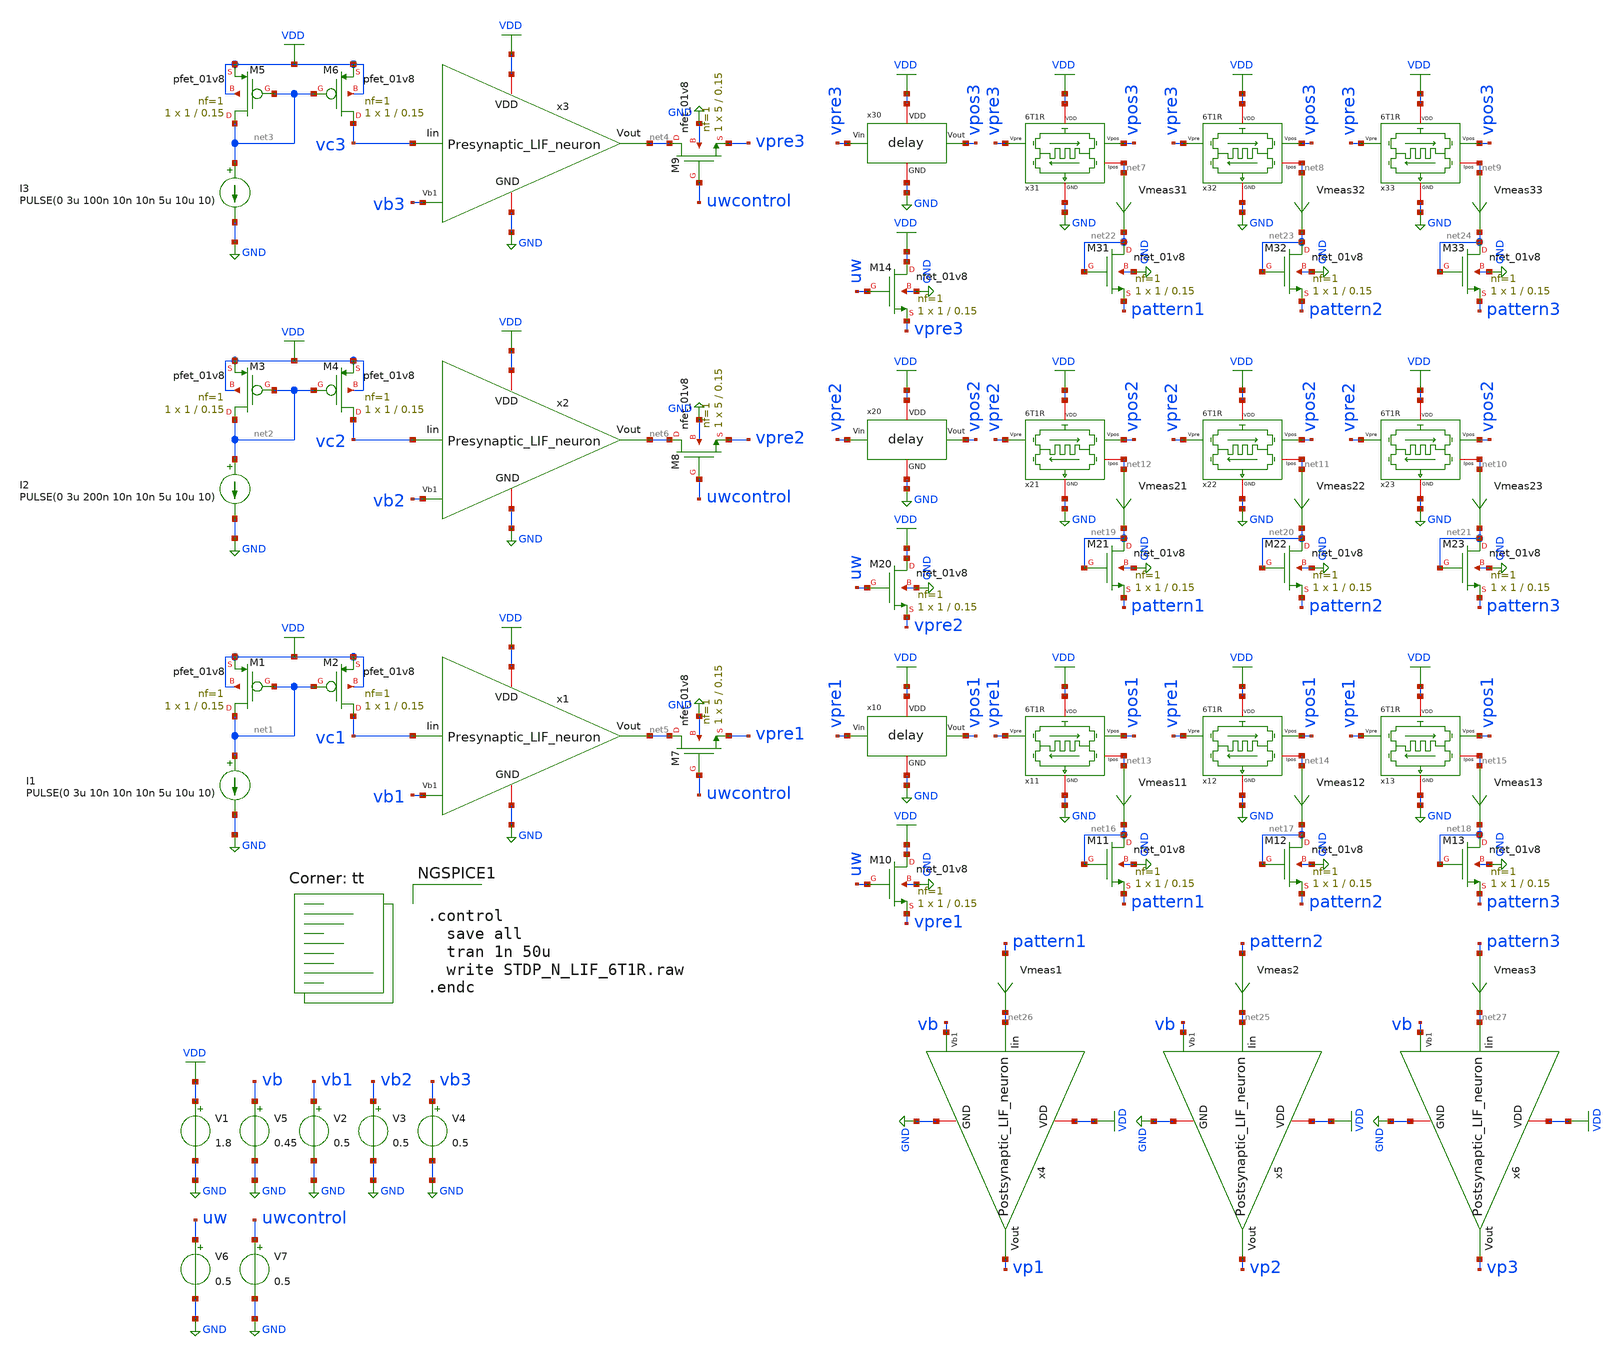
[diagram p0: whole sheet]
** sch_path: STDP/SNN_test.sch
**.subckt SNN_test
V1 VDD GND 1.8
V2 vb1 GND 0.5
I1 net1 GND PULSE(0 3u 10n 10n 10n 5u 10u 10)
XM2 vc1 net1 VDD VDD sky130_fd_pr__pfet_01v8 L=0.15 W=1 nf=1 ad='int((nf+1)/2) * W/nf * 0.29' as='int((nf+2)/2) * W/nf * 0.29'
+ pd='2*int((nf+1)/2) * (W/nf + 0.29)' ps='2*int((nf+2)/2) * (W/nf + 0.29)' nrd='0.29 / W' nrs='0.29 / W'
+ sa=0 sb=0 sd=0 mult=1 m=1
XM1 net1 net1 VDD VDD sky130_fd_pr__pfet_01v8 L=0.15 W=1 nf=1 ad='int((nf+1)/2) * W/nf * 0.29' as='int((nf+2)/2) * W/nf * 0.29'
+ pd='2*int((nf+1)/2) * (W/nf + 0.29)' ps='2*int((nf+2)/2) * (W/nf + 0.29)' nrd='0.29 / W' nrs='0.29 / W'
+ sa=0 sb=0 sd=0 mult=1 m=1
Vmeas31 net7 net22 0
.save i(vmeas31)
V3 vb2 GND 0.5
V4 vb3 GND 0.5
x1 VDD net5 vb1 GND vc1 Presynaptic_LIF_neuron
x5 net25 VDD vp2 vb GND Postsynaptic_LIF_neuron
V5 vb GND 0.45
x2 VDD net6 vb2 GND vc2 Presynaptic_LIF_neuron
I2 net2 GND PULSE(0 3u 200n 10n 10n 5u 10u 10)
XM4 vc2 net2 VDD VDD sky130_fd_pr__pfet_01v8 L=0.15 W=1 nf=1 ad='int((nf+1)/2) * W/nf * 0.29' as='int((nf+2)/2) * W/nf * 0.29'
+ pd='2*int((nf+1)/2) * (W/nf + 0.29)' ps='2*int((nf+2)/2) * (W/nf + 0.29)' nrd='0.29 / W' nrs='0.29 / W'
+ sa=0 sb=0 sd=0 mult=1 m=1
XM3 net2 net2 VDD VDD sky130_fd_pr__pfet_01v8 L=0.15 W=1 nf=1 ad='int((nf+1)/2) * W/nf * 0.29' as='int((nf+2)/2) * W/nf * 0.29'
+ pd='2*int((nf+1)/2) * (W/nf + 0.29)' ps='2*int((nf+2)/2) * (W/nf + 0.29)' nrd='0.29 / W' nrs='0.29 / W'
+ sa=0 sb=0 sd=0 mult=1 m=1
x31 VDD net7 vpre3 vpos3 GND 6T1R
x3 VDD net4 vb3 GND vc3 Presynaptic_LIF_neuron
I3 net3 GND PULSE(0 3u 100n 10n 10n 5u 10u 10)
XM6 vc3 net3 VDD VDD sky130_fd_pr__pfet_01v8 L=0.15 W=1 nf=1 ad='int((nf+1)/2) * W/nf * 0.29' as='int((nf+2)/2) * W/nf * 0.29'
+ pd='2*int((nf+1)/2) * (W/nf + 0.29)' ps='2*int((nf+2)/2) * (W/nf + 0.29)' nrd='0.29 / W' nrs='0.29 / W'
+ sa=0 sb=0 sd=0 mult=1 m=1
XM5 net3 net3 VDD VDD sky130_fd_pr__pfet_01v8 L=0.15 W=1 nf=1 ad='int((nf+1)/2) * W/nf * 0.29' as='int((nf+2)/2) * W/nf * 0.29'
+ pd='2*int((nf+1)/2) * (W/nf + 0.29)' ps='2*int((nf+2)/2) * (W/nf + 0.29)' nrd='0.29 / W' nrs='0.29 / W'
+ sa=0 sb=0 sd=0 mult=1 m=1
x30 VDD vpre3 vpos3 GND delay
XM9 net4 uwcontrol vpre3 GND sky130_fd_pr__nfet_01v8 L=0.15 W=5 nf=1 ad='int((nf+1)/2) * W/nf * 0.29'
+ as='int((nf+2)/2) * W/nf * 0.29' pd='2*int((nf+1)/2) * (W/nf + 0.29)' ps='2*int((nf+2)/2) * (W/nf + 0.29)'
+ nrd='0.29 / W' nrs='0.29 / W' sa=0 sb=0 sd=0 mult=1 m=1
XM8 net6 uwcontrol vpre2 GND sky130_fd_pr__nfet_01v8 L=0.15 W=5 nf=1 ad='int((nf+1)/2) * W/nf * 0.29'
+ as='int((nf+2)/2) * W/nf * 0.29' pd='2*int((nf+1)/2) * (W/nf + 0.29)' ps='2*int((nf+2)/2) * (W/nf + 0.29)'
+ nrd='0.29 / W' nrs='0.29 / W' sa=0 sb=0 sd=0 mult=1 m=1
XM7 net5 uwcontrol vpre1 GND sky130_fd_pr__nfet_01v8 L=0.15 W=5 nf=1 ad='int((nf+1)/2) * W/nf * 0.29'
+ as='int((nf+2)/2) * W/nf * 0.29' pd='2*int((nf+1)/2) * (W/nf + 0.29)' ps='2*int((nf+2)/2) * (W/nf + 0.29)'
+ nrd='0.29 / W' nrs='0.29 / W' sa=0 sb=0 sd=0 mult=1 m=1
x11 VDD net13 vpre1 vpos1 GND 6T1R
x10 VDD vpre1 vpos1 GND delay
x21 VDD net12 vpre2 vpos2 GND 6T1R
x20 VDD vpre2 vpos2 GND delay
x32 VDD net8 vpre3 vpos3 GND 6T1R
x12 VDD net14 vpre1 vpos1 GND 6T1R
x22 VDD net11 vpre2 vpos2 GND 6T1R
x33 VDD net9 vpre3 vpos3 GND 6T1R
x13 VDD net15 vpre1 vpos1 GND 6T1R
x23 VDD net10 vpre2 vpos2 GND 6T1R
Vmeas32 net8 net23 0
.save i(vmeas32)
Vmeas33 net9 net24 0
.save i(vmeas33)
Vmeas23 net10 net21 0
.save i(vmeas23)
Vmeas22 net11 net20 0
.save i(vmeas22)
Vmeas21 net12 net19 0
.save i(vmeas21)
Vmeas11 net13 net16 0
.save i(vmeas11)
Vmeas12 net14 net17 0
.save i(vmeas12)
Vmeas13 net15 net18 0
.save i(vmeas13)
XM11 net16 net16 pattern1 GND sky130_fd_pr__nfet_01v8 L=0.15 W=1 nf=1 ad='int((nf+1)/2) * W/nf * 0.29'
+ as='int((nf+2)/2) * W/nf * 0.29' pd='2*int((nf+1)/2) * (W/nf + 0.29)' ps='2*int((nf+2)/2) * (W/nf + 0.29)'
+ nrd='0.29 / W' nrs='0.29 / W' sa=0 sb=0 sd=0 mult=1 m=1
XM12 net17 net17 pattern2 GND sky130_fd_pr__nfet_01v8 L=0.15 W=1 nf=1 ad='int((nf+1)/2) * W/nf * 0.29'
+ as='int((nf+2)/2) * W/nf * 0.29' pd='2*int((nf+1)/2) * (W/nf + 0.29)' ps='2*int((nf+2)/2) * (W/nf + 0.29)'
+ nrd='0.29 / W' nrs='0.29 / W' sa=0 sb=0 sd=0 mult=1 m=1
XM13 net18 net18 pattern3 GND sky130_fd_pr__nfet_01v8 L=0.15 W=1 nf=1 ad='int((nf+1)/2) * W/nf * 0.29'
+ as='int((nf+2)/2) * W/nf * 0.29' pd='2*int((nf+1)/2) * (W/nf + 0.29)' ps='2*int((nf+2)/2) * (W/nf + 0.29)'
+ nrd='0.29 / W' nrs='0.29 / W' sa=0 sb=0 sd=0 mult=1 m=1
XM21 net19 net19 pattern1 GND sky130_fd_pr__nfet_01v8 L=0.15 W=1 nf=1 ad='int((nf+1)/2) * W/nf * 0.29'
+ as='int((nf+2)/2) * W/nf * 0.29' pd='2*int((nf+1)/2) * (W/nf + 0.29)' ps='2*int((nf+2)/2) * (W/nf + 0.29)'
+ nrd='0.29 / W' nrs='0.29 / W' sa=0 sb=0 sd=0 mult=1 m=1
XM22 net20 net20 pattern2 GND sky130_fd_pr__nfet_01v8 L=0.15 W=1 nf=1 ad='int((nf+1)/2) * W/nf * 0.29'
+ as='int((nf+2)/2) * W/nf * 0.29' pd='2*int((nf+1)/2) * (W/nf + 0.29)' ps='2*int((nf+2)/2) * (W/nf + 0.29)'
+ nrd='0.29 / W' nrs='0.29 / W' sa=0 sb=0 sd=0 mult=1 m=1
XM23 net21 net21 pattern3 GND sky130_fd_pr__nfet_01v8 L=0.15 W=1 nf=1 ad='int((nf+1)/2) * W/nf * 0.29'
+ as='int((nf+2)/2) * W/nf * 0.29' pd='2*int((nf+1)/2) * (W/nf + 0.29)' ps='2*int((nf+2)/2) * (W/nf + 0.29)'
+ nrd='0.29 / W' nrs='0.29 / W' sa=0 sb=0 sd=0 mult=1 m=1
XM31 net22 net22 pattern1 GND sky130_fd_pr__nfet_01v8 L=0.15 W=1 nf=1 ad='int((nf+1)/2) * W/nf * 0.29'
+ as='int((nf+2)/2) * W/nf * 0.29' pd='2*int((nf+1)/2) * (W/nf + 0.29)' ps='2*int((nf+2)/2) * (W/nf + 0.29)'
+ nrd='0.29 / W' nrs='0.29 / W' sa=0 sb=0 sd=0 mult=1 m=1
XM32 net23 net23 pattern2 GND sky130_fd_pr__nfet_01v8 L=0.15 W=1 nf=1 ad='int((nf+1)/2) * W/nf * 0.29'
+ as='int((nf+2)/2) * W/nf * 0.29' pd='2*int((nf+1)/2) * (W/nf + 0.29)' ps='2*int((nf+2)/2) * (W/nf + 0.29)'
+ nrd='0.29 / W' nrs='0.29 / W' sa=0 sb=0 sd=0 mult=1 m=1
XM33 net24 net24 pattern3 GND sky130_fd_pr__nfet_01v8 L=0.15 W=1 nf=1 ad='int((nf+1)/2) * W/nf * 0.29'
+ as='int((nf+2)/2) * W/nf * 0.29' pd='2*int((nf+1)/2) * (W/nf + 0.29)' ps='2*int((nf+2)/2) * (W/nf + 0.29)'
+ nrd='0.29 / W' nrs='0.29 / W' sa=0 sb=0 sd=0 mult=1 m=1
XM10 VDD uw vpre1 GND sky130_fd_pr__nfet_01v8 L=0.15 W=1 nf=1 ad='int((nf+1)/2) * W/nf * 0.29' as='int((nf+2)/2) * W/nf * 0.29'
+ pd='2*int((nf+1)/2) * (W/nf + 0.29)' ps='2*int((nf+2)/2) * (W/nf + 0.29)' nrd='0.29 / W' nrs='0.29 / W'
+ sa=0 sb=0 sd=0 mult=1 m=1
XM20 VDD uw vpre2 GND sky130_fd_pr__nfet_01v8 L=0.15 W=1 nf=1 ad='int((nf+1)/2) * W/nf * 0.29' as='int((nf+2)/2) * W/nf * 0.29'
+ pd='2*int((nf+1)/2) * (W/nf + 0.29)' ps='2*int((nf+2)/2) * (W/nf + 0.29)' nrd='0.29 / W' nrs='0.29 / W'
+ sa=0 sb=0 sd=0 mult=1 m=1
XM14 VDD uw vpre3 GND sky130_fd_pr__nfet_01v8 L=0.15 W=1 nf=1 ad='int((nf+1)/2) * W/nf * 0.29' as='int((nf+2)/2) * W/nf * 0.29'
+ pd='2*int((nf+1)/2) * (W/nf + 0.29)' ps='2*int((nf+2)/2) * (W/nf + 0.29)' nrd='0.29 / W' nrs='0.29 / W'
+ sa=0 sb=0 sd=0 mult=1 m=1
Vmeas2 pattern2 net25 0
.save i(vmeas2)
x4 net26 VDD vp1 vb GND Postsynaptic_LIF_neuron
Vmeas1 pattern1 net26 0
.save i(vmeas1)
x6 net27 VDD vp3 vb GND Postsynaptic_LIF_neuron
Vmeas3 pattern3 net27 0
.save i(vmeas3)
V6 uw GND 0.5
V7 uwcontrol GND 0.5
**** begin user architecture code
.lib $::SKYWATER_MODELS/sky130.lib.spice tt

** opencircuitdesign pdks install
.inc $::SKYWATER_MODELS/rram_v0.spice



.control
  save all
  tran 1n 50u
  write STDP_N_LIF_6T1R.raw
.endc


**** end user architecture code
**.ends

* expanding   symbol:
*+  /home/ricardo/RATT_repos/Proyectos_xschem/LIF_neuron/Presynaptic_LIF_neuron.sym # of pins=5
** sym_path: LIF_neuron/Presynaptic_LIF_neuron.sym
** sch_path: LIF_neuron/Presynaptic_LIF_neuron.sch
.subckt Presynaptic_LIF_neuron VDD Vout Vb1 GND Iin
*.iopin GND
*.ipin Vb1
*.iopin VDD
*.opin Vout
*.ipin Iin
XM13 net2 Vb1 GND GND sky130_fd_pr__nfet_01v8 L=0.5 W=5 nf=1 ad='int((nf+1)/2) * W/nf * 0.29' as='int((nf+2)/2) * W/nf * 0.29'
+ pd='2*int((nf+1)/2) * (W/nf + 0.29)' ps='2*int((nf+2)/2) * (W/nf + 0.29)' nrd='0.29 / W' nrs='0.29 / W'
+ sa=0 sb=0 sd=0 mult=1 m=1
XM12 Crefr net1 net2 GND sky130_fd_pr__nfet_01v8 L=1 W=1 nf=1 ad='int((nf+1)/2) * W/nf * 0.29' as='int((nf+2)/2) * W/nf * 0.29'
+ pd='2*int((nf+1)/2) * (W/nf + 0.29)' ps='2*int((nf+2)/2) * (W/nf + 0.29)' nrd='0.29 / W' nrs='0.29 / W'
+ sa=0 sb=0 sd=0 mult=1 m=1
XM11 Crefr net1 VDD VDD sky130_fd_pr__pfet_01v8 L=1 W=1 nf=1 ad='int((nf+1)/2) * W/nf * 0.29' as='int((nf+2)/2) * W/nf * 0.29'
+ pd='2*int((nf+1)/2) * (W/nf + 0.29)' ps='2*int((nf+2)/2) * (W/nf + 0.29)' nrd='0.29 / W' nrs='0.29 / W'
+ sa=0 sb=0 sd=0 mult=1 m=1
XCrefr Crefr GND sky130_fd_pr__cap_mim_m3_1 W=10 L=1 MF=1 m=1
XM14 Iin Crefr GND GND sky130_fd_pr__nfet_01v8 L=7 W=0.45 nf=1 ad='int((nf+1)/2) * W/nf * 0.29' as='int((nf+2)/2) * W/nf * 0.29'
+ pd='2*int((nf+1)/2) * (W/nf + 0.29)' ps='2*int((nf+2)/2) * (W/nf + 0.29)' nrd='0.29 / W' nrs='0.29 / W'
+ sa=0 sb=0 sd=0 mult=1 m=1
XCm Iin GND sky130_fd_pr__cap_mim_m3_1 W=10 L=1 MF=10 m=10
XM6 net3 Vout GND GND sky130_fd_pr__nfet_01v8 L=0.5 W=1 nf=1 ad='int((nf+1)/2) * W/nf * 0.29' as='int((nf+2)/2) * W/nf * 0.29'
+ pd='2*int((nf+1)/2) * (W/nf + 0.29)' ps='2*int((nf+2)/2) * (W/nf + 0.29)' nrd='0.29 / W' nrs='0.29 / W'
+ sa=0 sb=0 sd=0 mult=1 m=1
XM7 net1 Iin net3 GND sky130_fd_pr__nfet_01v8 L=1 W=1 nf=1 ad='int((nf+1)/2) * W/nf * 0.29' as='int((nf+2)/2) * W/nf * 0.29'
+ pd='2*int((nf+1)/2) * (W/nf + 0.29)' ps='2*int((nf+2)/2) * (W/nf + 0.29)' nrd='0.29 / W' nrs='0.29 / W'
+ sa=0 sb=0 sd=0 mult=1 m=1
XM8 net1 Iin VDD VDD sky130_fd_pr__pfet_01v8 L=1 W=1 nf=1 ad='int((nf+1)/2) * W/nf * 0.29' as='int((nf+2)/2) * W/nf * 0.29'
+ pd='2*int((nf+1)/2) * (W/nf + 0.29)' ps='2*int((nf+2)/2) * (W/nf + 0.29)' nrd='0.29 / W' nrs='0.29 / W'
+ sa=0 sb=0 sd=0 mult=1 m=1
XM9 Vout net1 net3 GND sky130_fd_pr__nfet_01v8 L=1 W=1 nf=1 ad='int((nf+1)/2) * W/nf * 0.29' as='int((nf+2)/2) * W/nf * 0.29'
+ pd='2*int((nf+1)/2) * (W/nf + 0.29)' ps='2*int((nf+2)/2) * (W/nf + 0.29)' nrd='0.29 / W' nrs='0.29 / W'
+ sa=0 sb=0 sd=0 mult=1 m=1
XM10 Vout net1 VDD VDD sky130_fd_pr__pfet_01v8 L=1 W=5 nf=1 ad='int((nf+1)/2) * W/nf * 0.29' as='int((nf+2)/2) * W/nf * 0.29'
+ pd='2*int((nf+1)/2) * (W/nf + 0.29)' ps='2*int((nf+2)/2) * (W/nf + 0.29)' nrd='0.29 / W' nrs='0.29 / W'
+ sa=0 sb=0 sd=0 mult=1 m=1
.ends


* expanding   symbol:
*+  /home/ricardo/RATT_repos/Proyectos_xschem/LIF_neuron/Postsynaptic_LIF_neuron.sym # of pins=5
** sym_path: LIF_neuron/Postsynaptic_LIF_neuron.sym
** sch_path: LIF_neuron/Postsynaptic_LIF_neuron.sch
.subckt Postsynaptic_LIF_neuron Iin VDD Vout Vb1 GND
*.iopin GND
*.ipin Vb1
*.iopin VDD
*.opin Vout
*.ipin Iin
XM13 net2 Vb1 GND GND sky130_fd_pr__nfet_01v8 L=0.5 W=5 nf=1 ad='int((nf+1)/2) * W/nf * 0.29' as='int((nf+2)/2) * W/nf * 0.29'
+ pd='2*int((nf+1)/2) * (W/nf + 0.29)' ps='2*int((nf+2)/2) * (W/nf + 0.29)' nrd='0.29 / W' nrs='0.29 / W'
+ sa=0 sb=0 sd=0 mult=1 m=1
XM12 Crefr net1 net2 GND sky130_fd_pr__nfet_01v8 L=1 W=1 nf=1 ad='int((nf+1)/2) * W/nf * 0.29' as='int((nf+2)/2) * W/nf * 0.29'
+ pd='2*int((nf+1)/2) * (W/nf + 0.29)' ps='2*int((nf+2)/2) * (W/nf + 0.29)' nrd='0.29 / W' nrs='0.29 / W'
+ sa=0 sb=0 sd=0 mult=1 m=1
XM11 Crefr net1 VDD VDD sky130_fd_pr__pfet_01v8 L=1 W=1 nf=1 ad='int((nf+1)/2) * W/nf * 0.29' as='int((nf+2)/2) * W/nf * 0.29'
+ pd='2*int((nf+1)/2) * (W/nf + 0.29)' ps='2*int((nf+2)/2) * (W/nf + 0.29)' nrd='0.29 / W' nrs='0.29 / W'
+ sa=0 sb=0 sd=0 mult=1 m=1
XC1 Crefr GND sky130_fd_pr__cap_mim_m3_1 W=21 L=1 MF=1 m=1
XM14 Iin Crefr GND GND sky130_fd_pr__nfet_01v8 L=40 W=1 nf=1 ad='int((nf+1)/2) * W/nf * 0.29' as='int((nf+2)/2) * W/nf * 0.29'
+ pd='2*int((nf+1)/2) * (W/nf + 0.29)' ps='2*int((nf+2)/2) * (W/nf + 0.29)' nrd='0.29 / W' nrs='0.29 / W'
+ sa=0 sb=0 sd=0 mult=1 m=1
XC2 Iin GND sky130_fd_pr__cap_mim_m3_1 W=20 L=1 MF=50 m=50
XM6 net3 Vout GND GND sky130_fd_pr__nfet_01v8 L=0.5 W=1 nf=1 ad='int((nf+1)/2) * W/nf * 0.29' as='int((nf+2)/2) * W/nf * 0.29'
+ pd='2*int((nf+1)/2) * (W/nf + 0.29)' ps='2*int((nf+2)/2) * (W/nf + 0.29)' nrd='0.29 / W' nrs='0.29 / W'
+ sa=0 sb=0 sd=0 mult=1 m=1
XM7 net1 Iin net3 GND sky130_fd_pr__nfet_01v8 L=1 W=1 nf=1 ad='int((nf+1)/2) * W/nf * 0.29' as='int((nf+2)/2) * W/nf * 0.29'
+ pd='2*int((nf+1)/2) * (W/nf + 0.29)' ps='2*int((nf+2)/2) * (W/nf + 0.29)' nrd='0.29 / W' nrs='0.29 / W'
+ sa=0 sb=0 sd=0 mult=1 m=1
XM8 net1 Iin VDD VDD sky130_fd_pr__pfet_01v8 L=1 W=1 nf=1 ad='int((nf+1)/2) * W/nf * 0.29' as='int((nf+2)/2) * W/nf * 0.29'
+ pd='2*int((nf+1)/2) * (W/nf + 0.29)' ps='2*int((nf+2)/2) * (W/nf + 0.29)' nrd='0.29 / W' nrs='0.29 / W'
+ sa=0 sb=0 sd=0 mult=1 m=1
XM9 Vout net1 net3 GND sky130_fd_pr__nfet_01v8 L=1 W=1 nf=1 ad='int((nf+1)/2) * W/nf * 0.29' as='int((nf+2)/2) * W/nf * 0.29'
+ pd='2*int((nf+1)/2) * (W/nf + 0.29)' ps='2*int((nf+2)/2) * (W/nf + 0.29)' nrd='0.29 / W' nrs='0.29 / W'
+ sa=0 sb=0 sd=0 mult=1 m=1
XM10 Vout net1 VDD VDD sky130_fd_pr__pfet_01v8 L=1 W=5 nf=1 ad='int((nf+1)/2) * W/nf * 0.29' as='int((nf+2)/2) * W/nf * 0.29'
+ pd='2*int((nf+1)/2) * (W/nf + 0.29)' ps='2*int((nf+2)/2) * (W/nf + 0.29)' nrd='0.29 / W' nrs='0.29 / W'
+ sa=0 sb=0 sd=0 mult=1 m=1
.ends


* expanding   symbol:  /home/ricardo/RATT_repos/Proyectos_xschem/synapse/6T1R.sym # of pins=5
** sym_path: synapse/6T1R.sym
** sch_path: synapse/6T1R.sch
.subckt 6T1R VDD Ipos Vpre Vpos GND
*.ipin Vpre
*.ipin Vpos
*.iopin GND
*.iopin Ipos
*.iopin VDD
XM1 BE Vpre vipre GND sky130_fd_pr__nfet_01v8 L=0.15 W=1 nf=1 ad='int((nf+1)/2) * W/nf * 0.29' as='int((nf+2)/2) * W/nf * 0.29'
+ pd='2*int((nf+1)/2) * (W/nf + 0.29)' ps='2*int((nf+2)/2) * (W/nf + 0.29)' nrd='0.29 / W' nrs='0.29 / W'
+ sa=0 sb=0 sd=0 mult=1 m=1
XR1 TE BE rram_v0
XM3 TE Vpos vipre GND sky130_fd_pr__nfet_01v8 L=0.15 W=20 nf=1 ad='int((nf+1)/2) * W/nf * 0.29' as='int((nf+2)/2) * W/nf * 0.29'
+ pd='2*int((nf+1)/2) * (W/nf + 0.29)' ps='2*int((nf+2)/2) * (W/nf + 0.29)' nrd='0.29 / W' nrs='0.29 / W'
+ sa=0 sb=0 sd=0 mult=1 m=1
XM6 Ipos vipre VDD VDD sky130_fd_pr__pfet_01v8 L=0.15 W=20 nf=1 ad='int((nf+1)/2) * W/nf * 0.29' as='int((nf+2)/2) * W/nf * 0.29'
+ pd='2*int((nf+1)/2) * (W/nf + 0.29)' ps='2*int((nf+2)/2) * (W/nf + 0.29)' nrd='0.29 / W' nrs='0.29 / W'
+ sa=0 sb=0 sd=0 mult=1 m=1
XM5 vipre vipre VDD VDD sky130_fd_pr__pfet_01v8 L=0.15 W=20 nf=1 ad='int((nf+1)/2) * W/nf * 0.29' as='int((nf+2)/2) * W/nf * 0.29'
+ pd='2*int((nf+1)/2) * (W/nf + 0.29)' ps='2*int((nf+2)/2) * (W/nf + 0.29)' nrd='0.29 / W' nrs='0.29 / W'
+ sa=0 sb=0 sd=0 mult=1 m=1
XM2 GND Vpos BE GND sky130_fd_pr__nfet_01v8 L=0.15 W=20 nf=1 ad='int((nf+1)/2) * W/nf * 0.29' as='int((nf+2)/2) * W/nf * 0.29'
+ pd='2*int((nf+1)/2) * (W/nf + 0.29)' ps='2*int((nf+2)/2) * (W/nf + 0.29)' nrd='0.29 / W' nrs='0.29 / W'
+ sa=0 sb=0 sd=0 mult=1 m=1
XM4 GND Vpre TE GND sky130_fd_pr__nfet_01v8 L=0.15 W=1 nf=1 ad='int((nf+1)/2) * W/nf * 0.29' as='int((nf+2)/2) * W/nf * 0.29'
+ pd='2*int((nf+1)/2) * (W/nf + 0.29)' ps='2*int((nf+2)/2) * (W/nf + 0.29)' nrd='0.29 / W' nrs='0.29 / W'
+ sa=0 sb=0 sd=0 mult=1 m=1
.ends


* expanding   symbol:  /home/ricardo/RATT_repos/Proyectos_xschem/delay/delay.sym # of pins=4
** sym_path: delay/delay.sym
** sch_path: delay/delay.sch
.subckt delay VDD Vin Vout GND
*.ipin Vin
*.opin Vout
*.iopin VDD
*.iopin GND
XM1 net1 Vin VDD VDD sky130_fd_pr__pfet_01v8 L=10 W=0.5 nf=1 ad='int((nf+1)/2) * W/nf * 0.29' as='int((nf+2)/2) * W/nf * 0.29'
+ pd='2*int((nf+1)/2) * (W/nf + 0.29)' ps='2*int((nf+2)/2) * (W/nf + 0.29)' nrd='0.29 / W' nrs='0.29 / W'
+ sa=0 sb=0 sd=0 mult=1 m=1
XM2 net1 Vin GND GND sky130_fd_pr__nfet_01v8 L=10 W=0.5 nf=1 ad='int((nf+1)/2) * W/nf * 0.29' as='int((nf+2)/2) * W/nf * 0.29'
+ pd='2*int((nf+1)/2) * (W/nf + 0.29)' ps='2*int((nf+2)/2) * (W/nf + 0.29)' nrd='0.29 / W' nrs='0.29 / W'
+ sa=0 sb=0 sd=0 mult=1 m=1
XM3 net2 net1 VDD VDD sky130_fd_pr__pfet_01v8 L=10 W=0.5 nf=1 ad='int((nf+1)/2) * W/nf * 0.29' as='int((nf+2)/2) * W/nf * 0.29'
+ pd='2*int((nf+1)/2) * (W/nf + 0.29)' ps='2*int((nf+2)/2) * (W/nf + 0.29)' nrd='0.29 / W' nrs='0.29 / W'
+ sa=0 sb=0 sd=0 mult=1 m=1
XM4 net2 net1 GND GND sky130_fd_pr__nfet_01v8 L=10 W=0.5 nf=1 ad='int((nf+1)/2) * W/nf * 0.29' as='int((nf+2)/2) * W/nf * 0.29'
+ pd='2*int((nf+1)/2) * (W/nf + 0.29)' ps='2*int((nf+2)/2) * (W/nf + 0.29)' nrd='0.29 / W' nrs='0.29 / W'
+ sa=0 sb=0 sd=0 mult=1 m=1
XM5 net3 net2 VDD VDD sky130_fd_pr__pfet_01v8 L=10 W=0.5 nf=1 ad='int((nf+1)/2) * W/nf * 0.29' as='int((nf+2)/2) * W/nf * 0.29'
+ pd='2*int((nf+1)/2) * (W/nf + 0.29)' ps='2*int((nf+2)/2) * (W/nf + 0.29)' nrd='0.29 / W' nrs='0.29 / W'
+ sa=0 sb=0 sd=0 mult=1 m=1
XM6 net3 net2 GND GND sky130_fd_pr__nfet_01v8 L=10 W=0.5 nf=1 ad='int((nf+1)/2) * W/nf * 0.29' as='int((nf+2)/2) * W/nf * 0.29'
+ pd='2*int((nf+1)/2) * (W/nf + 0.29)' ps='2*int((nf+2)/2) * (W/nf + 0.29)' nrd='0.29 / W' nrs='0.29 / W'
+ sa=0 sb=0 sd=0 mult=1 m=1
XM7 Vout net3 VDD VDD sky130_fd_pr__pfet_01v8 L=10 W=0.5 nf=1 ad='int((nf+1)/2) * W/nf * 0.29' as='int((nf+2)/2) * W/nf * 0.29'
+ pd='2*int((nf+1)/2) * (W/nf + 0.29)' ps='2*int((nf+2)/2) * (W/nf + 0.29)' nrd='0.29 / W' nrs='0.29 / W'
+ sa=0 sb=0 sd=0 mult=1 m=1
XM8 Vout net3 GND GND sky130_fd_pr__nfet_01v8 L=10 W=0.5 nf=1 ad='int((nf+1)/2) * W/nf * 0.29' as='int((nf+2)/2) * W/nf * 0.29'
+ pd='2*int((nf+1)/2) * (W/nf + 0.29)' ps='2*int((nf+2)/2) * (W/nf + 0.29)' nrd='0.29 / W' nrs='0.29 / W'
+ sa=0 sb=0 sd=0 mult=1 m=1
.ends

.GLOBAL GND
.GLOBAL VDD
.end
